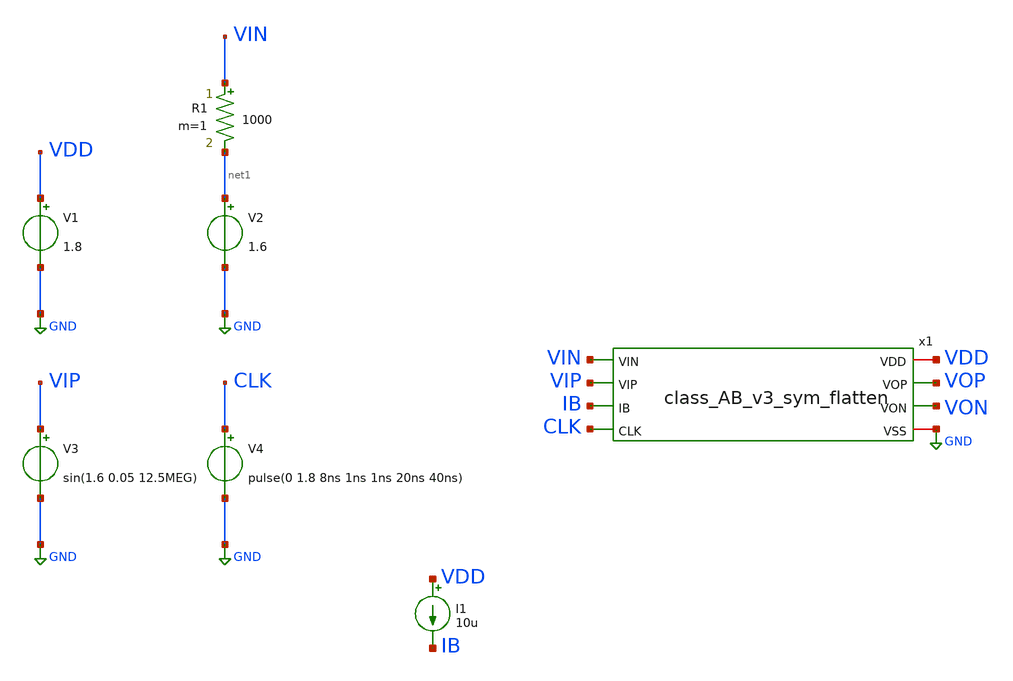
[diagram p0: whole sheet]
** sch_path: ComparatorLayout/xschem/class_AB_v3_testple.sch
.lib $::SKYWATER_MODELS/sky130.lib.spice tt
.include $::SKYWATER_STDCELLS/sky130_fd_sc_hd.spice

**.subckt class_AB_v3_testple
V1 VDD GND 1.8
V3 VIP GND sin(1.6 0.05 12.5MEG)
V2 net1 GND 1.6
V4 CLK GND pulse(0 1.8 8ns 1ns 1ns 20ns 40ns)
R1 VIN net1 1000 m=1
I1 VDD IB 10u
x1 VDD VOP VON VIN VIP IB CLK GND class_AB_v3_sym_flatten
**** begin user architecture code

.include /foss/designs/Analog_FA23_SP24/ComparatorLayout/magicple/class_AB_v3_sym_flatten.spice


.options savecurrents
.control

save all

tran 0.001n 120n
remzerovec
write class_AB_v3_testple.raw

.endc


**** end user architecture code
**.ends
.GLOBAL GND
.end
